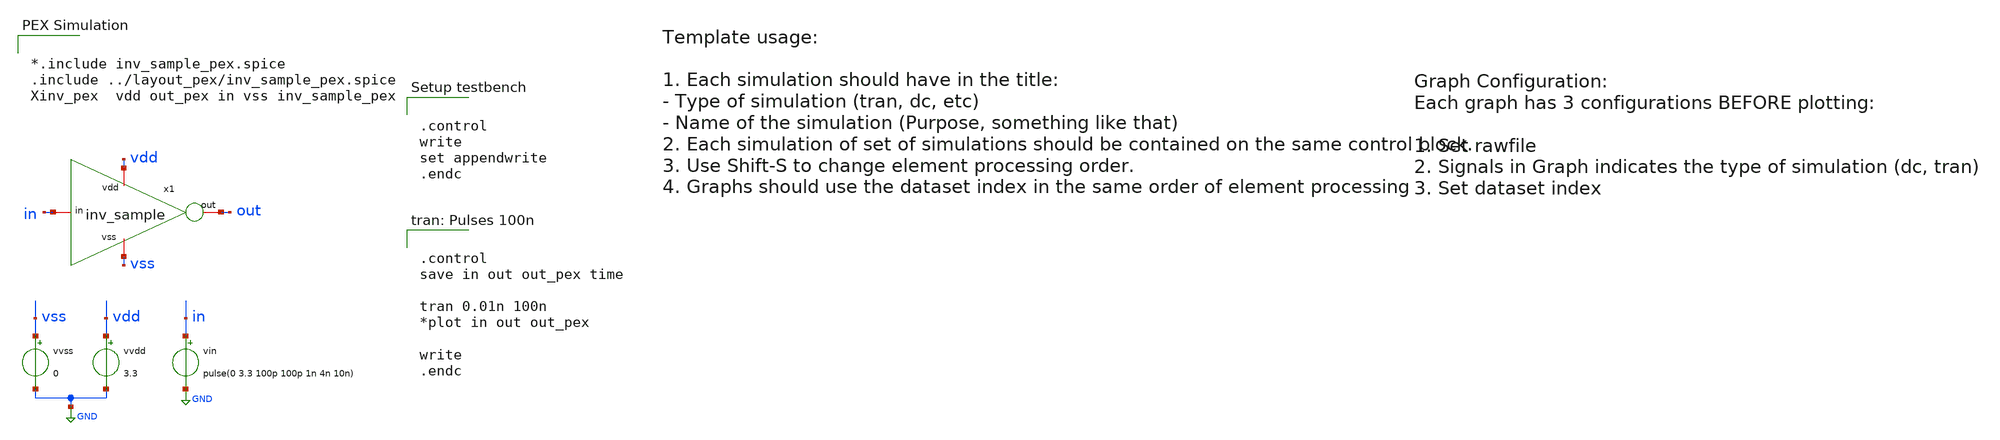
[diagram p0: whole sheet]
** sch_path: samples/gf180mcu/inv_sample/test/inv_sample_test.sch

.include $env(PDK_ROOT)/$env(PDK)/libs.tech/ngspice/design.ngspice
.lib $env(PDK_ROOT)/$env(PDK)/libs.tech/ngspice/sm141064.ngspice typical
.lib $env(PDK_ROOT)/$env(PDK)/libs.tech/ngspice/sm141064.ngspice mimcap_statistical
.lib $env(PDK_ROOT)/$env(PDK)/libs.tech/ngspice/sm141064.ngspice cap_mim
.lib $env(PDK_ROOT)/$env(PDK)/libs.tech/ngspice/sm141064.ngspice res_typical
.lib $env(PDK_ROOT)/$env(PDK)/libs.tech/ngspice/sm141064.ngspice bjt_typical
.lib $env(PDK_ROOT)/$env(PDK)/libs.tech/ngspice/sm141064.ngspice moscap_typical


.control
write
set appendwrite
.endc


**.subckt inv_sample_test
x1 vdd out in vss inv_sample
vvdd vdd GND 3.3
vin in GND pulse(0 3.3 100p 100p 1n 4n 10n)
vvss vss GND 0
**** begin user architecture code


.control
save in out out_pex time

tran 0.01n 100n
*plot in out out_pex

write
.endc




.control
save in out out_pex time

tran 0.01n 20n
*plot in out out_pex

write
.endc




*.include inv_sample_pex.spice
.include ../layout_pex/inv_sample_pex.spice
Xinv_pex  vdd out_pex in vss inv_sample_pex




.control
save in out out_pex

dc vin 0 3.3 0.001
*plot out vs in out_pex vs in

write
.endc


**** end user architecture code
**.ends

* expanding   symbol:  symbol/inv_sample.sym # of pins=4
** sym_path: samples/inv_sample/symbol/inv_sample.sym
** sch_path: samples/inv_sample/symbol/inv_sample.sch
.subckt inv_sample vdd out in vss
*.iopin vdd
*.iopin out
*.iopin vss
*.iopin in
XM1 out in vdd vdd pfet_03v3 L=0.28u W=1.26u nf=1 ad='int((nf+1)/2) * W/nf * 0.18u' as='int((nf+2)/2) * W/nf * 0.18u'
+ pd='2*int((nf+1)/2) * (W/nf + 0.18u)' ps='2*int((nf+2)/2) * (W/nf + 0.18u)' nrd='0.18u / W' nrs='0.18u / W'
+ sa=0 sb=0 sd=0 m=1
XM2 out in vss vss nfet_03v3 L=0.28u W=0.42u nf=1 ad='int((nf+1)/2) * W/nf * 0.18u' as='int((nf+2)/2) * W/nf * 0.18u'
+ pd='2*int((nf+1)/2) * (W/nf + 0.18u)' ps='2*int((nf+2)/2) * (W/nf + 0.18u)' nrd='0.18u / W' nrs='0.18u / W'
+ sa=0 sb=0 sd=0 m=1
.ends

.GLOBAL GND
.end
